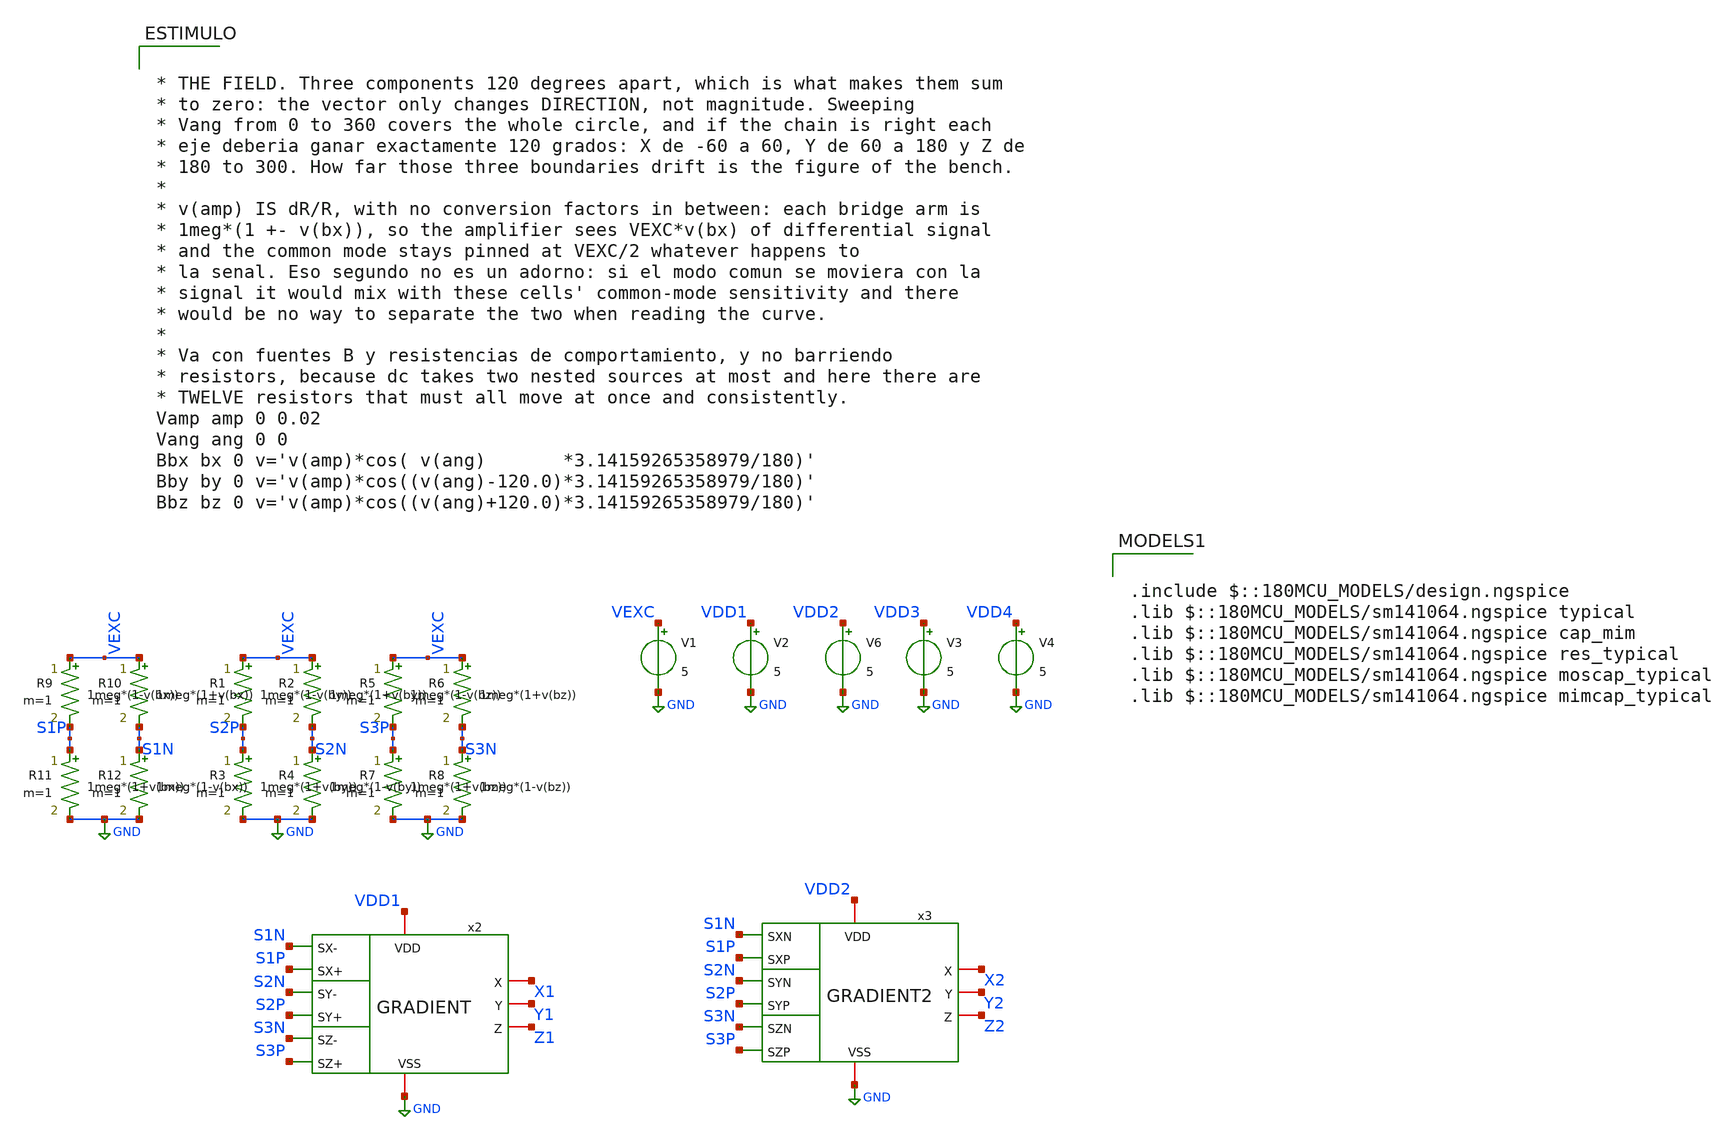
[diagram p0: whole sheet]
** sch_path: FINAL/XSCHEM/TEST_TOTAL/test_GRADIENT.sch
**.subckt test_GRADIENT
V1 VEXC GND 5
V2 VDD1 GND 5
V6 VDD2 GND 5
x2 S1N S1P VDD1 X1 S2N Y1 Z1 S2P GND S3N S3P GRADIENT
x3 S1N S1P VDD2 X2 S2N Y2 Z2 S2P GND S3N S3P GRADIENT2
R1 VEXC S2P r=' 1meg*(1-v(by)) '
R2 VEXC S2N r=' 1meg*(1+v(by)) '
R3 S2P GND r=' 1meg*(1+v(by)) '
R4 S2N GND r=' 1meg*(1-v(by)) '
V3 VDD3 GND 5
V4 VDD4 GND 5
R5 VEXC S3P r=' 1meg*(1-v(bz)) '
R6 VEXC S3N r=' 1meg*(1+v(bz)) '
R7 S3P GND r=' 1meg*(1+v(bz)) '
R8 S3N GND r=' 1meg*(1-v(bz)) '
R9 VEXC S1P r=' 1meg*(1-v(bx)) '
R10 VEXC S1N r=' 1meg*(1+v(bx)) '
R11 S1P GND r=' 1meg*(1+v(bx)) '
R12 S1N GND r=' 1meg*(1-v(bx)) '
**** begin user architecture code

.include $::180MCU_MODELS/design.ngspice
.lib $::180MCU_MODELS/sm141064.ngspice typical
.lib $::180MCU_MODELS/sm141064.ngspice cap_mim
.lib $::180MCU_MODELS/sm141064.ngspice res_typical
.lib $::180MCU_MODELS/sm141064.ngspice moscap_typical
.lib $::180MCU_MODELS/sm141064.ngspice mimcap_typical



* THE FIELD. Three components 120 degrees apart, which is what makes them sum
* to zero: the vector only changes DIRECTION, not magnitude. Sweeping
* Vang from 0 to 360 covers the whole circle, and if the chain is right each
* eje deberia ganar exactamente 120 grados: X de -60 a 60, Y de 60 a 180 y Z de
* 180 to 300. How far those three boundaries drift is the figure of the bench.
*
* v(amp) IS dR/R, with no conversion factors in between: each bridge arm is
* 1meg*(1 +- v(bx)), so the amplifier sees VEXC*v(bx) of differential signal
* and the common mode stays pinned at VEXC/2 whatever happens to
* la senal. Eso segundo no es un adorno: si el modo comun se moviera con la
* signal it would mix with these cells' common-mode sensitivity and there
* would be no way to separate the two when reading the curve.
*
* Va con fuentes B y resistencias de comportamiento, y no barriendo
* resistors, because dc takes two nested sources at most and here there are
* TWELVE resistors that must all move at once and consistently.
Vamp amp 0 0.02
Vang ang 0 0
Bbx bx 0 v='v(amp)*cos( v(ang)       *3.14159265358979/180)'
Bby by 0 v='v(amp)*cos((v(ang)-120.0)*3.14159265358979/180)'
Bbz bz 0 v='v(amp)*cos((v(ang)+120.0)*3.14159265358979/180)'




* THE SAME TWO CHAINS, REBUILT FROM THE v2 LAYOUT BLOCKS.
* They hang off the SAME six sensor nodes as the schematic ones and each
* carries its own supply, so current draw can be compared too.
*
* La topologia es la de COMBINATION/GRADIENT.sch, copiada nodo a nodo:
*
*     amp X: S1N->INN  S1P->INP  -> SX        COMP XY: INN=SX INP=SY -> XY
*     amp Y: S2N->INN  S2P->INP  -> SY        COMP XZ: INN=SX INP=SZ -> XZ
*     amp Z: S3N->INN  S3P->INP  -> SZ        COMP YZ: INN=SY INP=SZ -> YZ
*                                             DECODER: XY XZ YZ -> X Y Z
*
* CAREFUL WITH THE PORT ORDER. xschem emits them in the order of the symbol B
* lines and magic in the order it finds them in the layout, and they do NOT agree:
* el esquematico declara OPAM VDD INN OUT INP VSS y el extraido OPAM VSS VDD OUT
* INP INN. Cablear las dos igual significa cosas distintas y no da ningun error.
* That is why the real order is written above each group, and why the files are
* the _V2_ ones produced by TEST/preparar_extraidos.sh: it renames the subcircuit
* -- both declare the same name and cannot be included together -- and normalises
* the order. Note that OPAM_LIN_flat has OUT in the middle and the others do not.
.include ../../../../layouts_v2/OPAM/mag/OPAM_V2_pex_rc.spice
.include ../../../../layouts_v2/OPAM_LIN_flat/mag/OPAM_LIN_flat_V2_pex_rc.spice
.include ../../../../layouts_v2/COMP/mag/COMP_V2_pex_rc.spice
.include ../../../../layouts_v2/DECODER/mag/DECODER_V2_pex_rc.spice

* --- G3: the G1 chain, with the v2 layout OPAM
* .subckt OPAM_V2     VSS VDD OUT INP INN
XA31 GND VDD3 SX3 S1P S1N OPAM_V2
XA32 GND VDD3 SY3 S2P S2N OPAM_V2
XA33 GND VDD3 SZ3 S3P S3N OPAM_V2
* .subckt COMP_V2     VSS VDD OUT INP INN
XC31 GND VDD3 XY3 SY3 SX3 COMP_V2
XC32 GND VDD3 XZ3 SZ3 SX3 COMP_V2
XC33 GND VDD3 YZ3 SZ3 SY3 COMP_V2
* .subckt DECODER_V2  VSS VDD YZ Z XY XZ Y X
XD3  GND VDD3 YZ3 Z3 XY3 XZ3 Y3 X3 DECODER_V2

* --- G4: the G2 chain, with the v2 layout OPAM_LIN_flat
* .subckt OPAM_LIN_flat_V2  VSS VDD INP OUT INN
XA41 GND VDD4 S1P SX4 S1N OPAM_LIN_flat_V2
XA42 GND VDD4 S2P SY4 S2N OPAM_LIN_flat_V2
XA43 GND VDD4 S3P SZ4 S3N OPAM_LIN_flat_V2
* .subckt COMP_V2     VSS VDD OUT INP INN
XC41 GND VDD4 XY4 SY4 SX4 COMP_V2
XC42 GND VDD4 XZ4 SZ4 SX4 COMP_V2
XC43 GND VDD4 YZ4 SZ4 SY4 COMP_V2
* .subckt DECODER_V2  VSS VDD YZ Z XY XZ Y X
XD4  GND VDD4 YZ4 Z4 XY4 XZ4 Y4 X4 DECODER_V2




* CAREFUL: not one brace in this text. xschem counts them to find where the
* attribute block ends and a single one inside a comment cuts it in half,
* leaving the netlist with the template 'blabla' and raising no error.
*
* This bench does NOT need a common-mode source, unlike test_comp_* and
* test_opam_*: there the input pair were two gates with no DC path to
* ground, and here the bridge itself provides it.
*
* The intermediate signals of the schematic chains come out by hierarchical
* name, v(x2.SX) and company. In the hand-rebuilt ones the nodes are
* primer nivel y se llaman SX3, XY3 y asi.
.save all
.control
* Fondo de escala de una AMR tipica: dR/R = 2 %, o sea 100 mV diferenciales.
alter Vamp = 0.02
dc Vang 0 360 0.5
wrdata ancho.txt v(X1) v(Y1) v(Z1) v(X2) v(Y2) v(Z2) v(X3) v(Y3) v(Z3) v(X4) v(Y4) v(Z4) v(x2.SX) v(x2.SY) v(x2.SZ) v(x3.SX) v(x3.SY) v(x3.SZ) v(SX3) v(SY3) v(SZ3) v(SX4) v(SY4) v(SZ4) v(x2.net1) v(x2.net2) v(x2.net3) v(x3.net1) v(x3.net2) v(x3.net3) v(XY3) v(XZ3) v(YZ3) v(XY4) v(XZ4) v(YZ4) v(S1P) v(S1N) v(S2P) v(S2N) v(S3P) v(S3N) v(VEXC)*i(V1) v(VDD1)*i(V2) v(VDD2)*i(V6) v(VDD3)*i(V3) v(VDD4)*i(V4)
* Ventana fina: dR/R = 50 ppm, o sea 250 uV diferenciales.
alter Vamp = 50u
dc Vang 0 360 0.5
wrdata fino.txt v(X1) v(Y1) v(Z1) v(X2) v(Y2) v(Z2) v(X3) v(Y3) v(Z3) v(X4) v(Y4) v(Z4) v(x2.SX) v(x2.SY) v(x2.SZ) v(x3.SX) v(x3.SY) v(x3.SZ) v(SX3) v(SY3) v(SZ3) v(SX4) v(SY4) v(SZ4) v(x2.net1) v(x2.net2) v(x2.net3) v(x3.net1) v(x3.net2) v(x3.net3) v(XY3) v(XZ3) v(YZ3) v(XY4) v(XZ4) v(YZ4) v(S1P) v(S1N) v(S2P) v(S2N) v(S3P) v(S3N) v(VEXC)*i(V1) v(VDD1)*i(V2) v(VDD2)*i(V6) v(VDD3)*i(V3) v(VDD4)*i(V4)
.endc


**** end user architecture code
**.ends
.GLOBAL GND
.end
